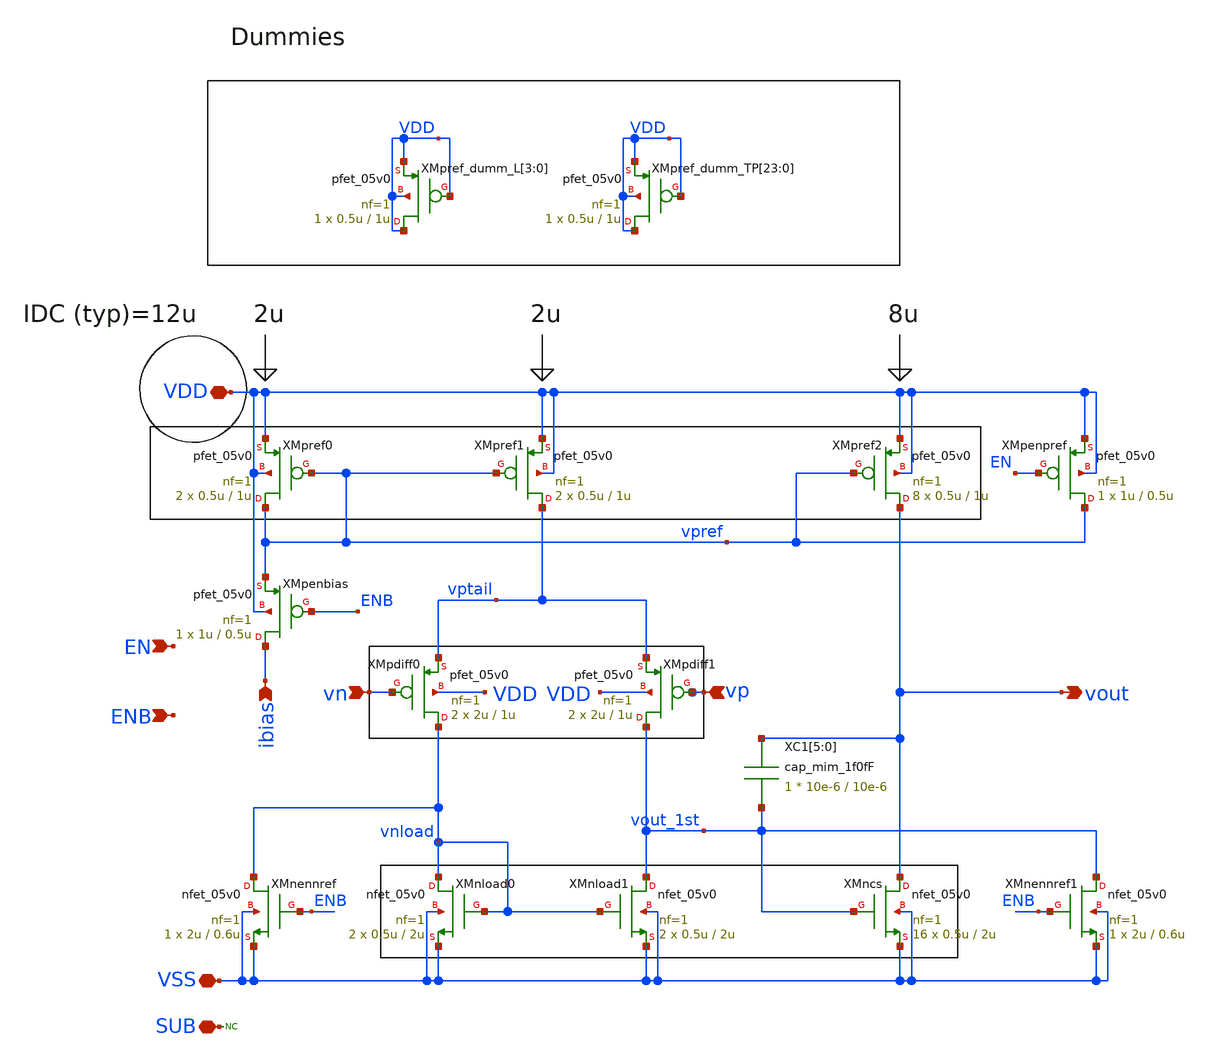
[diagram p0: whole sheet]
** sch_path: designs/libs/core_biasgen/biasgen_opamp/biasgen_opamp.sch
**.subckt biasgen_opamp vn vp vout ibias VDD VSS EN ENB SUB
*.ipin vn
*.ipin vp
*.opin vout
*.ipin ibias
*.iopin VDD
*.iopin VSS
*.ipin EN
*.ipin ENB
*.iopin SUB
XMpref0 vpref vpref VDD VDD pfet_05v0 L=1u W=0.5u nf=1 ad='int((nf+1)/2) * W/nf * 0.18u' as='int((nf+2)/2) * W/nf * 0.18u'
+ pd='2*int((nf+1)/2) * (W/nf + 0.18u)' ps='2*int((nf+2)/2) * (W/nf + 0.18u)' nrd='0.18u / W' nrs='0.18u / W'
+ sa=0 sb=0 sd=0 m=2
XMnload0 vnload vnload VSS VSS nfet_05v0 L=2u W=0.5u nf=1 ad='int((nf+1)/2) * W/nf * 0.18u' as='int((nf+2)/2) * W/nf * 0.18u'
+ pd='2*int((nf+1)/2) * (W/nf + 0.18u)' ps='2*int((nf+2)/2) * (W/nf + 0.18u)' nrd='0.18u / W' nrs='0.18u / W'
+ sa=0 sb=0 sd=0 m=2
XMpref1 vptail vpref VDD VDD pfet_05v0 L=1u W=0.5u nf=1 ad='int((nf+1)/2) * W/nf * 0.18u' as='int((nf+2)/2) * W/nf * 0.18u'
+ pd='2*int((nf+1)/2) * (W/nf + 0.18u)' ps='2*int((nf+2)/2) * (W/nf + 0.18u)' nrd='0.18u / W' nrs='0.18u / W'
+ sa=0 sb=0 sd=0 m=2
XMpref2 vout vpref VDD VDD pfet_05v0 L=1u W=0.5u nf=1 ad='int((nf+1)/2) * W/nf * 0.18u' as='int((nf+2)/2) * W/nf * 0.18u'
+ pd='2*int((nf+1)/2) * (W/nf + 0.18u)' ps='2*int((nf+2)/2) * (W/nf + 0.18u)' nrd='0.18u / W' nrs='0.18u / W'
+ sa=0 sb=0 sd=0 m=8
XMpdiff0 vnload vn vptail VDD pfet_05v0 L=1u W=2u nf=1 ad='int((nf+1)/2) * W/nf * 0.18u' as='int((nf+2)/2) * W/nf * 0.18u'
+ pd='2*int((nf+1)/2) * (W/nf + 0.18u)' ps='2*int((nf+2)/2) * (W/nf + 0.18u)' nrd='0.18u / W' nrs='0.18u / W'
+ sa=0 sb=0 sd=0 m=2
XMpdiff1 vout_1st vp vptail VDD pfet_05v0 L=1u W=2u nf=1 ad='int((nf+1)/2) * W/nf * 0.18u' as='int((nf+2)/2) * W/nf * 0.18u'
+ pd='2*int((nf+1)/2) * (W/nf + 0.18u)' ps='2*int((nf+2)/2) * (W/nf + 0.18u)' nrd='0.18u / W' nrs='0.18u / W'
+ sa=0 sb=0 sd=0 m=2
XMnload1 vout_1st vnload VSS VSS nfet_05v0 L=2u W=0.5u nf=1 ad='int((nf+1)/2) * W/nf * 0.18u' as='int((nf+2)/2) * W/nf * 0.18u'
+ pd='2*int((nf+1)/2) * (W/nf + 0.18u)' ps='2*int((nf+2)/2) * (W/nf + 0.18u)' nrd='0.18u / W' nrs='0.18u / W'
+ sa=0 sb=0 sd=0 m=2
XMncs vout vout_1st VSS VSS nfet_05v0 L=2u W=0.5u nf=1 ad='int((nf+1)/2) * W/nf * 0.18u' as='int((nf+2)/2) * W/nf * 0.18u'
+ pd='2*int((nf+1)/2) * (W/nf + 0.18u)' ps='2*int((nf+2)/2) * (W/nf + 0.18u)' nrd='0.18u / W' nrs='0.18u / W'
+ sa=0 sb=0 sd=0 m=16
XMpref_dumm_L[3] VDD VDD VDD VDD pfet_05v0 L=1u W=0.5u nf=1 ad='int((nf+1)/2) * W/nf * 0.18u' as='int((nf+2)/2) * W/nf * 0.18u'
+ pd='2*int((nf+1)/2) * (W/nf + 0.18u)' ps='2*int((nf+2)/2) * (W/nf + 0.18u)' nrd='0.18u / W' nrs='0.18u / W'
+ sa=0 sb=0 sd=0 m=1
XMpref_dumm_L[2] VDD VDD VDD VDD pfet_05v0 L=1u W=0.5u nf=1 ad='int((nf+1)/2) * W/nf * 0.18u' as='int((nf+2)/2) * W/nf * 0.18u'
+ pd='2*int((nf+1)/2) * (W/nf + 0.18u)' ps='2*int((nf+2)/2) * (W/nf + 0.18u)' nrd='0.18u / W' nrs='0.18u / W'
+ sa=0 sb=0 sd=0 m=1
XMpref_dumm_L[1] VDD VDD VDD VDD pfet_05v0 L=1u W=0.5u nf=1 ad='int((nf+1)/2) * W/nf * 0.18u' as='int((nf+2)/2) * W/nf * 0.18u'
+ pd='2*int((nf+1)/2) * (W/nf + 0.18u)' ps='2*int((nf+2)/2) * (W/nf + 0.18u)' nrd='0.18u / W' nrs='0.18u / W'
+ sa=0 sb=0 sd=0 m=1
XMpref_dumm_L[0] VDD VDD VDD VDD pfet_05v0 L=1u W=0.5u nf=1 ad='int((nf+1)/2) * W/nf * 0.18u' as='int((nf+2)/2) * W/nf * 0.18u'
+ pd='2*int((nf+1)/2) * (W/nf + 0.18u)' ps='2*int((nf+2)/2) * (W/nf + 0.18u)' nrd='0.18u / W' nrs='0.18u / W'
+ sa=0 sb=0 sd=0 m=1
XMpref_dumm_TP[23] VDD VDD VDD VDD pfet_05v0 L=1u W=0.5u nf=1 ad='int((nf+1)/2) * W/nf * 0.18u' as='int((nf+2)/2) * W/nf * 0.18u'
+ pd='2*int((nf+1)/2) * (W/nf + 0.18u)' ps='2*int((nf+2)/2) * (W/nf + 0.18u)' nrd='0.18u / W' nrs='0.18u / W'
+ sa=0 sb=0 sd=0 m=1
XMpref_dumm_TP[22] VDD VDD VDD VDD pfet_05v0 L=1u W=0.5u nf=1 ad='int((nf+1)/2) * W/nf * 0.18u' as='int((nf+2)/2) * W/nf * 0.18u'
+ pd='2*int((nf+1)/2) * (W/nf + 0.18u)' ps='2*int((nf+2)/2) * (W/nf + 0.18u)' nrd='0.18u / W' nrs='0.18u / W'
+ sa=0 sb=0 sd=0 m=1
XMpref_dumm_TP[21] VDD VDD VDD VDD pfet_05v0 L=1u W=0.5u nf=1 ad='int((nf+1)/2) * W/nf * 0.18u' as='int((nf+2)/2) * W/nf * 0.18u'
+ pd='2*int((nf+1)/2) * (W/nf + 0.18u)' ps='2*int((nf+2)/2) * (W/nf + 0.18u)' nrd='0.18u / W' nrs='0.18u / W'
+ sa=0 sb=0 sd=0 m=1
XMpref_dumm_TP[20] VDD VDD VDD VDD pfet_05v0 L=1u W=0.5u nf=1 ad='int((nf+1)/2) * W/nf * 0.18u' as='int((nf+2)/2) * W/nf * 0.18u'
+ pd='2*int((nf+1)/2) * (W/nf + 0.18u)' ps='2*int((nf+2)/2) * (W/nf + 0.18u)' nrd='0.18u / W' nrs='0.18u / W'
+ sa=0 sb=0 sd=0 m=1
XMpref_dumm_TP[19] VDD VDD VDD VDD pfet_05v0 L=1u W=0.5u nf=1 ad='int((nf+1)/2) * W/nf * 0.18u' as='int((nf+2)/2) * W/nf * 0.18u'
+ pd='2*int((nf+1)/2) * (W/nf + 0.18u)' ps='2*int((nf+2)/2) * (W/nf + 0.18u)' nrd='0.18u / W' nrs='0.18u / W'
+ sa=0 sb=0 sd=0 m=1
XMpref_dumm_TP[18] VDD VDD VDD VDD pfet_05v0 L=1u W=0.5u nf=1 ad='int((nf+1)/2) * W/nf * 0.18u' as='int((nf+2)/2) * W/nf * 0.18u'
+ pd='2*int((nf+1)/2) * (W/nf + 0.18u)' ps='2*int((nf+2)/2) * (W/nf + 0.18u)' nrd='0.18u / W' nrs='0.18u / W'
+ sa=0 sb=0 sd=0 m=1
XMpref_dumm_TP[17] VDD VDD VDD VDD pfet_05v0 L=1u W=0.5u nf=1 ad='int((nf+1)/2) * W/nf * 0.18u' as='int((nf+2)/2) * W/nf * 0.18u'
+ pd='2*int((nf+1)/2) * (W/nf + 0.18u)' ps='2*int((nf+2)/2) * (W/nf + 0.18u)' nrd='0.18u / W' nrs='0.18u / W'
+ sa=0 sb=0 sd=0 m=1
XMpref_dumm_TP[16] VDD VDD VDD VDD pfet_05v0 L=1u W=0.5u nf=1 ad='int((nf+1)/2) * W/nf * 0.18u' as='int((nf+2)/2) * W/nf * 0.18u'
+ pd='2*int((nf+1)/2) * (W/nf + 0.18u)' ps='2*int((nf+2)/2) * (W/nf + 0.18u)' nrd='0.18u / W' nrs='0.18u / W'
+ sa=0 sb=0 sd=0 m=1
XMpref_dumm_TP[15] VDD VDD VDD VDD pfet_05v0 L=1u W=0.5u nf=1 ad='int((nf+1)/2) * W/nf * 0.18u' as='int((nf+2)/2) * W/nf * 0.18u'
+ pd='2*int((nf+1)/2) * (W/nf + 0.18u)' ps='2*int((nf+2)/2) * (W/nf + 0.18u)' nrd='0.18u / W' nrs='0.18u / W'
+ sa=0 sb=0 sd=0 m=1
XMpref_dumm_TP[14] VDD VDD VDD VDD pfet_05v0 L=1u W=0.5u nf=1 ad='int((nf+1)/2) * W/nf * 0.18u' as='int((nf+2)/2) * W/nf * 0.18u'
+ pd='2*int((nf+1)/2) * (W/nf + 0.18u)' ps='2*int((nf+2)/2) * (W/nf + 0.18u)' nrd='0.18u / W' nrs='0.18u / W'
+ sa=0 sb=0 sd=0 m=1
XMpref_dumm_TP[13] VDD VDD VDD VDD pfet_05v0 L=1u W=0.5u nf=1 ad='int((nf+1)/2) * W/nf * 0.18u' as='int((nf+2)/2) * W/nf * 0.18u'
+ pd='2*int((nf+1)/2) * (W/nf + 0.18u)' ps='2*int((nf+2)/2) * (W/nf + 0.18u)' nrd='0.18u / W' nrs='0.18u / W'
+ sa=0 sb=0 sd=0 m=1
XMpref_dumm_TP[12] VDD VDD VDD VDD pfet_05v0 L=1u W=0.5u nf=1 ad='int((nf+1)/2) * W/nf * 0.18u' as='int((nf+2)/2) * W/nf * 0.18u'
+ pd='2*int((nf+1)/2) * (W/nf + 0.18u)' ps='2*int((nf+2)/2) * (W/nf + 0.18u)' nrd='0.18u / W' nrs='0.18u / W'
+ sa=0 sb=0 sd=0 m=1
XMpref_dumm_TP[11] VDD VDD VDD VDD pfet_05v0 L=1u W=0.5u nf=1 ad='int((nf+1)/2) * W/nf * 0.18u' as='int((nf+2)/2) * W/nf * 0.18u'
+ pd='2*int((nf+1)/2) * (W/nf + 0.18u)' ps='2*int((nf+2)/2) * (W/nf + 0.18u)' nrd='0.18u / W' nrs='0.18u / W'
+ sa=0 sb=0 sd=0 m=1
XMpref_dumm_TP[10] VDD VDD VDD VDD pfet_05v0 L=1u W=0.5u nf=1 ad='int((nf+1)/2) * W/nf * 0.18u' as='int((nf+2)/2) * W/nf * 0.18u'
+ pd='2*int((nf+1)/2) * (W/nf + 0.18u)' ps='2*int((nf+2)/2) * (W/nf + 0.18u)' nrd='0.18u / W' nrs='0.18u / W'
+ sa=0 sb=0 sd=0 m=1
XMpref_dumm_TP[9] VDD VDD VDD VDD pfet_05v0 L=1u W=0.5u nf=1 ad='int((nf+1)/2) * W/nf * 0.18u' as='int((nf+2)/2) * W/nf * 0.18u'
+ pd='2*int((nf+1)/2) * (W/nf + 0.18u)' ps='2*int((nf+2)/2) * (W/nf + 0.18u)' nrd='0.18u / W' nrs='0.18u / W'
+ sa=0 sb=0 sd=0 m=1
XMpref_dumm_TP[8] VDD VDD VDD VDD pfet_05v0 L=1u W=0.5u nf=1 ad='int((nf+1)/2) * W/nf * 0.18u' as='int((nf+2)/2) * W/nf * 0.18u'
+ pd='2*int((nf+1)/2) * (W/nf + 0.18u)' ps='2*int((nf+2)/2) * (W/nf + 0.18u)' nrd='0.18u / W' nrs='0.18u / W'
+ sa=0 sb=0 sd=0 m=1
XMpref_dumm_TP[7] VDD VDD VDD VDD pfet_05v0 L=1u W=0.5u nf=1 ad='int((nf+1)/2) * W/nf * 0.18u' as='int((nf+2)/2) * W/nf * 0.18u'
+ pd='2*int((nf+1)/2) * (W/nf + 0.18u)' ps='2*int((nf+2)/2) * (W/nf + 0.18u)' nrd='0.18u / W' nrs='0.18u / W'
+ sa=0 sb=0 sd=0 m=1
XMpref_dumm_TP[6] VDD VDD VDD VDD pfet_05v0 L=1u W=0.5u nf=1 ad='int((nf+1)/2) * W/nf * 0.18u' as='int((nf+2)/2) * W/nf * 0.18u'
+ pd='2*int((nf+1)/2) * (W/nf + 0.18u)' ps='2*int((nf+2)/2) * (W/nf + 0.18u)' nrd='0.18u / W' nrs='0.18u / W'
+ sa=0 sb=0 sd=0 m=1
XMpref_dumm_TP[5] VDD VDD VDD VDD pfet_05v0 L=1u W=0.5u nf=1 ad='int((nf+1)/2) * W/nf * 0.18u' as='int((nf+2)/2) * W/nf * 0.18u'
+ pd='2*int((nf+1)/2) * (W/nf + 0.18u)' ps='2*int((nf+2)/2) * (W/nf + 0.18u)' nrd='0.18u / W' nrs='0.18u / W'
+ sa=0 sb=0 sd=0 m=1
XMpref_dumm_TP[4] VDD VDD VDD VDD pfet_05v0 L=1u W=0.5u nf=1 ad='int((nf+1)/2) * W/nf * 0.18u' as='int((nf+2)/2) * W/nf * 0.18u'
+ pd='2*int((nf+1)/2) * (W/nf + 0.18u)' ps='2*int((nf+2)/2) * (W/nf + 0.18u)' nrd='0.18u / W' nrs='0.18u / W'
+ sa=0 sb=0 sd=0 m=1
XMpref_dumm_TP[3] VDD VDD VDD VDD pfet_05v0 L=1u W=0.5u nf=1 ad='int((nf+1)/2) * W/nf * 0.18u' as='int((nf+2)/2) * W/nf * 0.18u'
+ pd='2*int((nf+1)/2) * (W/nf + 0.18u)' ps='2*int((nf+2)/2) * (W/nf + 0.18u)' nrd='0.18u / W' nrs='0.18u / W'
+ sa=0 sb=0 sd=0 m=1
XMpref_dumm_TP[2] VDD VDD VDD VDD pfet_05v0 L=1u W=0.5u nf=1 ad='int((nf+1)/2) * W/nf * 0.18u' as='int((nf+2)/2) * W/nf * 0.18u'
+ pd='2*int((nf+1)/2) * (W/nf + 0.18u)' ps='2*int((nf+2)/2) * (W/nf + 0.18u)' nrd='0.18u / W' nrs='0.18u / W'
+ sa=0 sb=0 sd=0 m=1
XMpref_dumm_TP[1] VDD VDD VDD VDD pfet_05v0 L=1u W=0.5u nf=1 ad='int((nf+1)/2) * W/nf * 0.18u' as='int((nf+2)/2) * W/nf * 0.18u'
+ pd='2*int((nf+1)/2) * (W/nf + 0.18u)' ps='2*int((nf+2)/2) * (W/nf + 0.18u)' nrd='0.18u / W' nrs='0.18u / W'
+ sa=0 sb=0 sd=0 m=1
XMpref_dumm_TP[0] VDD VDD VDD VDD pfet_05v0 L=1u W=0.5u nf=1 ad='int((nf+1)/2) * W/nf * 0.18u' as='int((nf+2)/2) * W/nf * 0.18u'
+ pd='2*int((nf+1)/2) * (W/nf + 0.18u)' ps='2*int((nf+2)/2) * (W/nf + 0.18u)' nrd='0.18u / W' nrs='0.18u / W'
+ sa=0 sb=0 sd=0 m=1
XMpenpref vpref EN VDD VDD pfet_05v0 L=0.5u W=1u nf=1 ad='int((nf+1)/2) * W/nf * 0.18u' as='int((nf+2)/2) * W/nf * 0.18u'
+ pd='2*int((nf+1)/2) * (W/nf + 0.18u)' ps='2*int((nf+2)/2) * (W/nf + 0.18u)' nrd='0.18u / W' nrs='0.18u / W'
+ sa=0 sb=0 sd=0 m=1
XMpenbias ibias ENB vpref VDD pfet_05v0 L=0.5u W=1u nf=1 ad='int((nf+1)/2) * W/nf * 0.18u' as='int((nf+2)/2) * W/nf * 0.18u'
+ pd='2*int((nf+1)/2) * (W/nf + 0.18u)' ps='2*int((nf+2)/2) * (W/nf + 0.18u)' nrd='0.18u / W' nrs='0.18u / W'
+ sa=0 sb=0 sd=0 m=1
XMnennref vnload ENB VSS VSS nfet_05v0 L=0.6u W=2u nf=1 ad='int((nf+1)/2) * W/nf * 0.18u' as='int((nf+2)/2) * W/nf * 0.18u'
+ pd='2*int((nf+1)/2) * (W/nf + 0.18u)' ps='2*int((nf+2)/2) * (W/nf + 0.18u)' nrd='0.18u / W' nrs='0.18u / W'
+ sa=0 sb=0 sd=0 m=1
XMnennref1 vout_1st ENB VSS VSS nfet_05v0 L=0.6u W=2u nf=1 ad='int((nf+1)/2) * W/nf * 0.18u' as='int((nf+2)/2) * W/nf * 0.18u'
+ pd='2*int((nf+1)/2) * (W/nf + 0.18u)' ps='2*int((nf+2)/2) * (W/nf + 0.18u)' nrd='0.18u / W' nrs='0.18u / W'
+ sa=0 sb=0 sd=0 m=1
* noconn SUB
XC1[5] vout vout_1st cap_mim_1f0fF c_width=10e-6 c_length=10e-6 m=1
XC1[4] vout vout_1st cap_mim_1f0fF c_width=10e-6 c_length=10e-6 m=1
XC1[3] vout vout_1st cap_mim_1f0fF c_width=10e-6 c_length=10e-6 m=1
XC1[2] vout vout_1st cap_mim_1f0fF c_width=10e-6 c_length=10e-6 m=1
XC1[1] vout vout_1st cap_mim_1f0fF c_width=10e-6 c_length=10e-6 m=1
XC1[0] vout vout_1st cap_mim_1f0fF c_width=10e-6 c_length=10e-6 m=1
**.ends
.end
